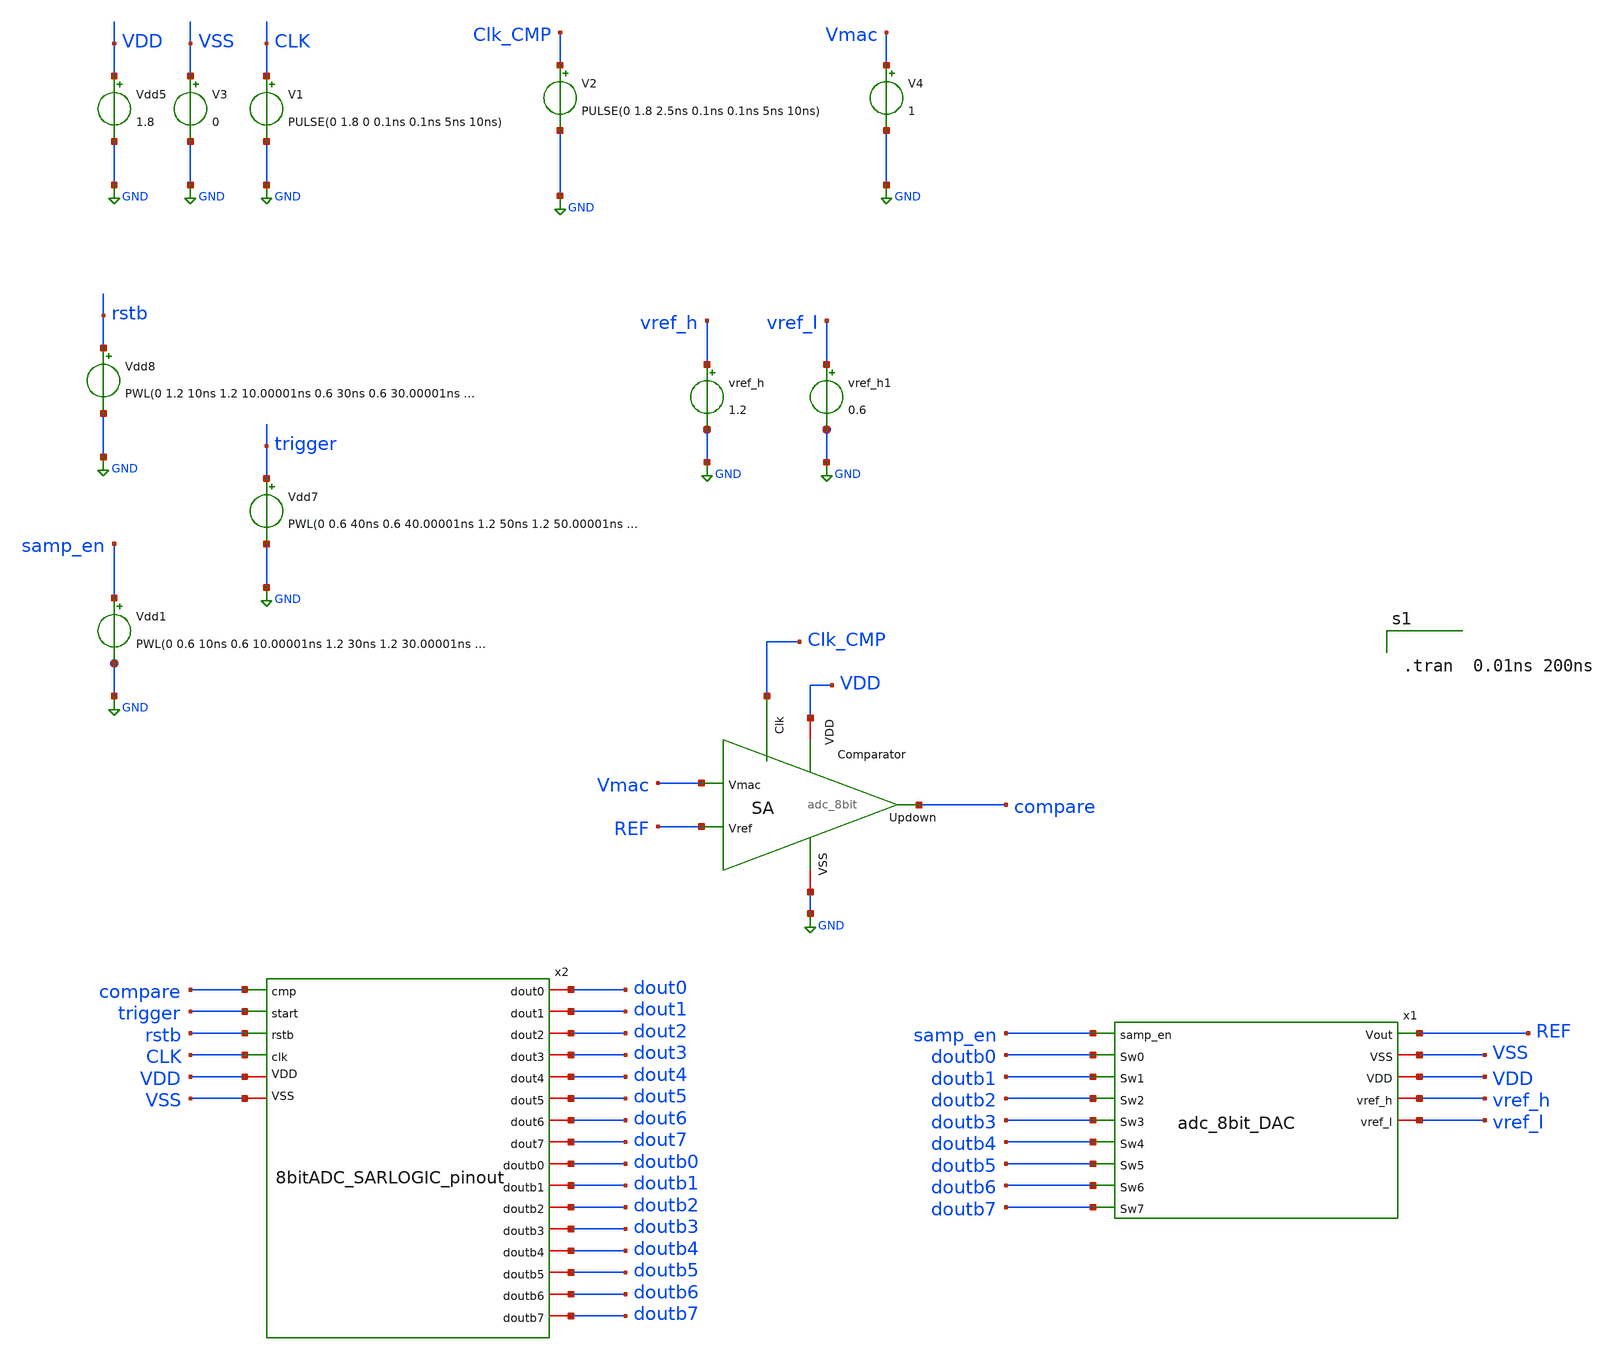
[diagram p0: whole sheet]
** sch_path: ADC_TB.sch
**.subckt ADC_TB
x1 REF VSS samp_en doutb0 VDD doutb1 vref_h doutb2 vref_l doutb3 doutb4 doutb5 doutb6 doutb7
+ adc_8bit_DAC
vref_h vref_h GND 1.2
Vdd5 VDD GND 1.8
V1 CLK GND PULSE(0 1.8 0 0.1ns 0.1ns 5ns 10ns)
V3 VSS GND 0
Vdd7 trigger GND PWL(0 0.6 40ns 0.6 40.00001ns 1.2 50ns 1.2 50.00001ns 0.6 )
Vdd8 rstb GND PWL(0 1.2 10ns 1.2 10.00001ns 0.6 30ns 0.6 30.00001ns 1.2 )
x3 GND VDD REF Clk_CMP Vmac compare adc_8bit
V4 Vmac GND 1
V2 Clk_CMP GND PULSE(0 1.8 2.5ns 0.1ns 0.1ns 5ns 10ns)
Vdd1 samp_en GND PWL(0 0.6 10ns 0.6 10.00001ns 1.2 30ns 1.2 30.00001ns 0.6 )
vref_h1 vref_l GND 0.6
x2 VDD compare VSS trigger doutb0 dout0 rstb CLK doutb1 dout1 doutb2 dout2 dout3 doutb3 dout4 doutb4
+ dout5 doutb5 dout6 doutb6 doutb7 dout7 8bitADC_SARLOGIC_pinout
**** begin user architecture code

** opencircuitdesign pdks install
.lib $::SKYWATER_MODELS/sky130.lib.spice tt
.include $::SKYWATER_STDCELLS/sky130_fd_sc_hd.spice



.tran  0.01ns 200ns



**** end user architecture code
**.ends
.GLOBAL GND
.end
